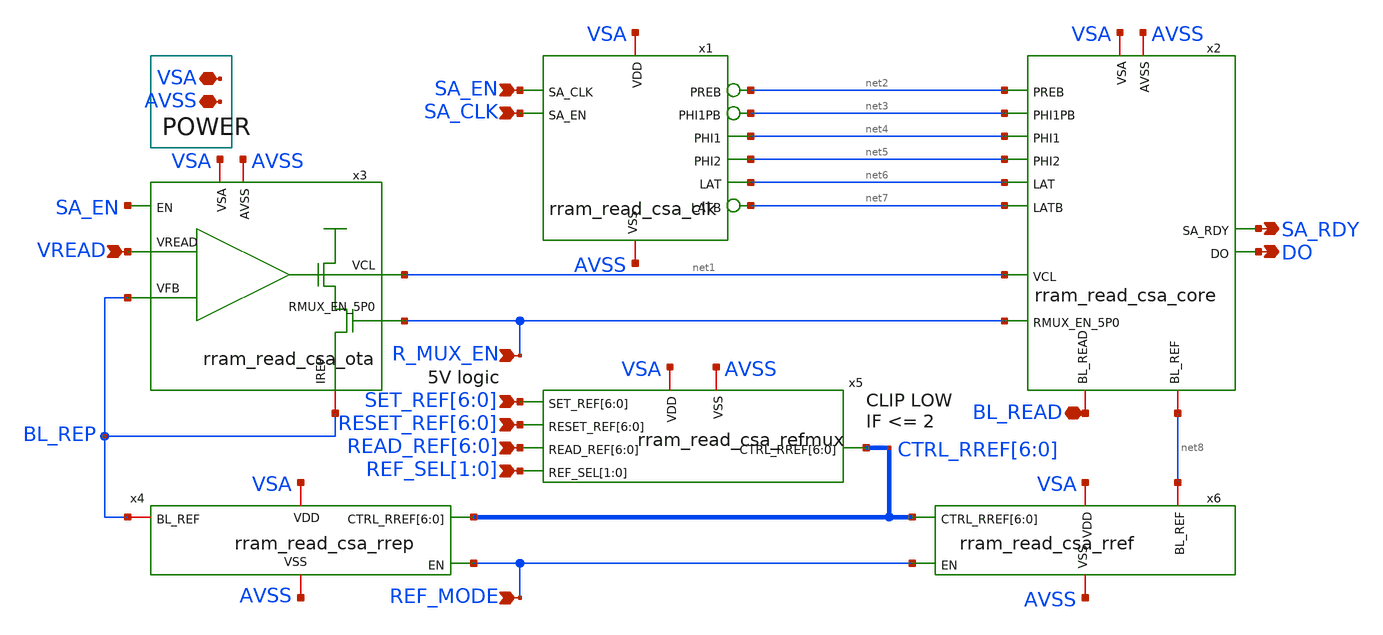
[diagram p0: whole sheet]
** sch_path: BL_Read_Interface/rram_read_csa.sch
**.subckt rram_read_csa VSA AVSS SA_EN SA_CLK VREAD R_MUX_EN
*+ SET_REF[6],SET_REF[5],SET_REF[4],SET_REF[3],SET_REF[2],SET_REF[1],SET_REF[0] REF_MODE SA_RDY DO BL_READ
*+ RESET_REF[6],RESET_REF[5],RESET_REF[4],RESET_REF[3],RESET_REF[2],RESET_REF[1],RESET_REF[0] READ_REF[6],READ_REF[5],READ_REF[4],READ_REF[3],READ_REF[2],READ_REF[1],READ_REF[0]
*+ REF_SEL[1],REF_SEL[0]
*.iopin VSA
*.iopin AVSS
*.ipin SA_EN
*.ipin SA_CLK
*.ipin VREAD
*.ipin R_MUX_EN
*.ipin SET_REF[6],SET_REF[5],SET_REF[4],SET_REF[3],SET_REF[2],SET_REF[1],SET_REF[0]
*.ipin REF_MODE
*.opin SA_RDY
*.opin DO
*.iopin BL_READ
*.ipin RESET_REF[6],RESET_REF[5],RESET_REF[4],RESET_REF[3],RESET_REF[2],RESET_REF[1],RESET_REF[0]
*.ipin READ_REF[6],READ_REF[5],READ_REF[4],READ_REF[3],READ_REF[2],READ_REF[1],READ_REF[0]
*.ipin REF_SEL[1],REF_SEL[0]
x1 SA_EN VSA AVSS SA_CLK net2 net3 net4 net5 net6 net7 rram_read_csa_clk
x2 SA_RDY DO VSA AVSS net2 net3 net4 net5 net6 net7 net1 R_MUX_EN BL_READ net8 rram_read_csa_core
x3 VSA BL_REP net1 VREAD SA_EN R_MUX_EN BL_REP AVSS rram_read_csa_ota
x4 BL_REP VSA CTRL_RREF[6] CTRL_RREF[5] CTRL_RREF[4] CTRL_RREF[3] CTRL_RREF[2] CTRL_RREF[1]
+ CTRL_RREF[0] REF_MODE AVSS rram_read_csa_rrep
x5 VSA AVSS SET_REF[6] SET_REF[5] SET_REF[4] SET_REF[3] SET_REF[2] SET_REF[1] SET_REF[0]
+ CTRL_RREF[6] CTRL_RREF[5] CTRL_RREF[4] CTRL_RREF[3] CTRL_RREF[2] CTRL_RREF[1] CTRL_RREF[0] RESET_REF[6]
+ RESET_REF[5] RESET_REF[4] RESET_REF[3] RESET_REF[2] RESET_REF[1] RESET_REF[0] READ_REF[6] READ_REF[5]
+ READ_REF[4] READ_REF[3] READ_REF[2] READ_REF[1] READ_REF[0] REF_SEL[1] REF_SEL[0] rram_read_csa_refmux
x6 net8 VSA CTRL_RREF[6] CTRL_RREF[5] CTRL_RREF[4] CTRL_RREF[3] CTRL_RREF[2] CTRL_RREF[1]
+ CTRL_RREF[0] REF_MODE AVSS rram_read_csa_rref
**.ends
.end
